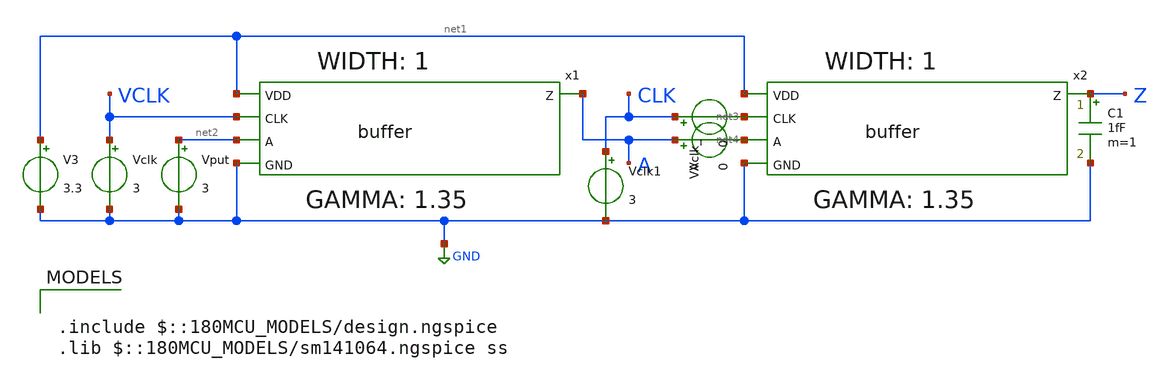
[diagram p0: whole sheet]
** sch_path: xschem/buffer_tb_delay.sch
**.subckt buffer_tb_delay
x2 net1 net3 Z net4 GND buffer
C1 Z GND 1fF m=1
Vput net2 GND 3
Vclk VCLK GND 3
V3 net1 GND 3.3
VA A net4 0
Vclk_ CLK net3 0
Vclk1 CLK GND 3
x1 net1 VCLK A net2 GND buffer
**** begin user architecture code

.include $::180MCU_MODELS/design.ngspice
.lib $::180MCU_MODELS/sm141064.ngspice ss

.control
* [[CITE]] High Performance ASIC Design: Using Synthesizable Domino Logic in an ASIC Flow, by Razak
*+ Hossain.
let vdd = 3.0v $ 3.0v at ss, 3.3v at typical, 3.6v at ff
let vhi = vdd * 0.8
let vlo = vdd * 0.2
let vtrip_fall = vdd * 0.6
let vtrip_rise = vdd * 0.4
let delay = 400ps
let pulse = 1400ps
let clock_pulse = delay + pulse
let temp = -40 $ -40 at ss, 25 at typical, 125 at ff
let tnom = 25

option temp=$&temp tnom=$&tnom

* 3.5.1 Cell delay and output transition time measurement:
* - Initially, all inputs are kept high.
* - The clock is then forced low.
* - After 400ps, all the data inputs are also driven low.
* - The output of a domino only goes low when the clock falls.
*   The fall delay for the cell is measured from the falling edge of the clock input.
* - To measure the rise delay, the related pins rise with the clock.
*   All other data pins remain off.
*   The PUT rises 200ps later.
* - For rise delay measurement from the clock pin, all relative pins rise at the same time as the
*+ clock.
* - The maximum input and clock transition used for characterisation is 150ps.
*   (a 150ps transition from 20% to 80% of Vdd is equivalent to a 250ps 0V to Vdd transition)
* - The maximum cell load used is the maximum capacitance value for the particular drive.
*   The maximum capacitance value is the capacitance load that leads to a 400ps (0 to 100% of Vdd)
*+ falling transition for a domino cell.
* - The delay and transition simulations are done for five different output loads and five different
*+ input transition times.

* 3.5.2 Input pin capacitance measurement
* - The input pin capacitance is measured by taking the integral of the current of the PUT's driving source and dividing it by Vdd.
*   Current is measured only when the signal is rising, and is recorded for each of the 25 delay measurement runs.
*   The average of all these values is then used.

* find maximum capacitance value for the cell
* => binary search on output capacitance such that trans_fall = 400ps
let c_max = 0.2pF
let c_min = 0pF
let c_out = c_min

let target_time = 400ps
let tolerance = 0.1ps
repeat
  set transition_time = 250ps
  let c_test = \{(c_max + c_min) / 2\}
  alter C1 cap = $&c_test
  alter Vclk pulse = [ $&vdd 0.0v 0s $transition_time $transition_time $&clock_pulse 100ns ]
  alter Vclk1 pulse = [ $&vdd 0.0v 0s $transition_time $transition_time $&clock_pulse 100ns ]
  alter Vput pulse = [ $&vdd 0.0v $&delay $transition_time $transition_time $&pulse 100ns ]
  tran 1ps 3ns
  meas tran trans_fall TRIG v(z) VAL=vhi FALL=1 TARG v(z) VAL=vlo FALL=1
  let abs_diff = \{abs(trans_fall - target_time)\}
  if abs_diff < tolerance
    let c_out = c_test
    break
  end
  if trans_fall > target_time
    let c_max = c_test
  else
    let c_min = c_test
  end
  reset
  option temp=$&temp tnom=$&tnom
end

echo -n > out.csv

echo output_cap z \{$&c_out\} >> out.csv

* characterise rise and fall delay and transition times
foreach capacitance_mul 0.2 0.4 0.6 0.8 1.0
  foreach transition_time 50ps 100ps 150ps 200ps 250ps
* input pin characterisation
    let transition_time = $transition_time
    let cap = c_out * $capacitance_mul
    alter C1 cap = $&cap
    alter Vclk pulse = [ $&vdd 0.0v 0s $&transition_time $&transition_time $&clock_pulse 100ns ]
    alter Vclk1 pulse = [ $&vdd 0.0v 0s $&transition_time $&transition_time $&clock_pulse 100ns ]
    alter Vput pulse = [ $&vdd 0.0v $&delay $&transition_time $&transition_time $&pulse 100ns ]
    tran 1ps 3ns

    meas tran delay_rise TRIG v(a) VAL=vtrip_rise RISE=1 TARG v(z) VAL=vtrip_rise RISE=1
    meas tran trans_fall TRIG v(z) VAL=vhi FALL=1 TARG v(z) VAL=vlo FALL=1
    meas tran trans_rise TRIG v(z) VAL=vlo RISE=1 TARG v(z) VAL=vhi RISE=1
    meas tran rise_start WHEN v(a)=vlo RISE=1
    meas tran rise_stop WHEN v(a)=vhi RISE=1
    meas tran charge INTEG i(VA) FROM=rise_start TO=rise_stop

    let transition_time = $transition_time
    let output_cap = c_out * $capacitance_mul
    let input_cap = charge / (vhi - vlo)

    echo delay_rise a z \{$&output_cap\} \{$&transition_time\} \{$&delay_rise\} >> out.csv
    echo trans_fall a z \{$&output_cap\} \{$&transition_time\} \{$&trans_fall\} >> out.csv
    echo trans_rise a z \{$&output_cap\} \{$&transition_time\} \{$&trans_rise\} >> out.csv
    echo input_cap a \{$&output_cap\} \{$&transition_time\} \{$&input_cap\} >> out.csv
    reset
    option temp=$&temp tnom=$&tnom

* clock characterisation
    let transition_time = $transition_time
    let cap = c_out * $capacitance_mul
    alter C1 cap = $&cap
    alter Vclk pulse = [ $&vdd 0.0v 0s $&transition_time $&transition_time $&clock_pulse 100ns ]
    alter Vclk1 pulse = [ $&vdd 0.0v 0s $&transition_time $&transition_time $&clock_pulse 100ns ]
    alter Vput pulse = [ $&vdd 0.0v 0s $&transition_time $&transition_time $&clock_pulse 100ns ]
    tran 1ps 3ns
    meas tran delay_fall TRIG v(clk) VAL=vtrip_fall FALL=1 TARG v(z) VAL=vtrip_fall FALL=1
    meas tran delay_rise TRIG v(clk) VAL=vtrip_rise RISE=1 TARG v(z) VAL=vtrip_rise RISE=1
    meas tran trans_fall TRIG v(z) VAL=vhi FALL=1 TARG v(z) VAL=vlo FALL=1
    meas tran trans_rise TRIG v(z) VAL=vlo RISE=1 TARG v(z) VAL=vhi RISE=1
    meas tran rise_start WHEN v(clk)=vlo RISE=1
    meas tran rise_stop WHEN v(clk)=vhi RISE=1
    meas tran charge INTEG i(VCLK_) FROM=rise_start TO=rise_stop

    let transition_time = $transition_time
    let output_cap = c_out * $capacitance_mul
    let input_cap = charge / (vhi - vlo)
    echo delay_fall clk z \{$&output_cap\} \{$&transition_time\} \{$&delay_fall\} >> out.csv
    echo delay_rise clk z \{$&output_cap\} \{$&transition_time\} \{$&delay_rise\} >> out.csv
    echo trans_fall clk z \{$&output_cap\} \{$&transition_time\} \{$&trans_fall\} >> out.csv
    echo trans_rise clk z \{$&output_cap\} \{$&transition_time\} \{$&trans_rise\} >> out.csv
    echo input_cap clk \{$&output_cap\} \{$&transition_time\} \{$&input_cap\} >> out.csv

    reset
    option temp=$&temp tnom=$&tnom
  end
end

* 3.5.3 Setup measurement of data input rising relative to the clock falling
* - The setup is defined to occur when the output fall delay decreases by 2.5% compared with the fall delays generated by a very large data setup time.
* - The clock initially goes low.
* - Related pins fall soon after.
* - Related pins and clock then rise simultaneously.
* - After a delay, the pin under test rises just before the clock falls.
* - This delay time when the PUT rises is then varied until the output fall delay is 97.5% of the original fall delay.

* characterise setup rise delay
* => binary search on setup such that pulse_width = delay_fall * 0.975
foreach transition_time 83ps 166ps 250ps
  foreach capacitance_mul 0.33 0.66 1.0
    set setup_max = 2000ps
    set setup_min = 260ps
    repeat 14 $ 0.106ps accuracy
      reset
      option temp=$&temp tnom=$&tnom

      let setup = ($setup_max + $setup_min) / 2.0
      let setup_time = 1400ps + (2000ps - setup)
      let transition_time = $transition_time
      let cap = c_out * $capacitance_mul
      alter C1 cap = $&cap
      alter Vclk pulse = [ $&vdd 0.0v 0s 250ps $&transition_time $&clock_pulse 3800ps ]
      alter Vclk1 pulse = [ $&vdd 0.0v 0s 250ps $&transition_time $&clock_pulse 3800ps ]
      alter Vput pulse = [ $&vdd 0.0v 400ps $&transition_time 250ps $&setup_time 100ns ]

      tran 1ps 5ns

      meas tran delay_fall TRIG v(clk) VAL=vtrip_fall FALL=1 TARG v(z) VAL=vtrip_fall FALL=1
      meas tran pulse_width TRIG v(z) VAL=vtrip_rise RISE=1 TARG v(z) VAL=vtrip_fall FALL=2
      meas tran setup_time TRIG v(a) VAL=vtrip_rise RISE=1 TARG v(clk) VAL=vtrip_fall FALL=2

      let pulse_width_target = delay_fall * 0.975
      let abs_diff = \{abs(pulse_width_target - pulse_width)\}
      if abs_diff < tolerance
        break
      end

      if pulse_width > pulse_width_target
        let _setup_max = ($setup_max + $setup_min) / 2.0
        set setup_max = $&_setup_max
      else
        let _setup_min = ($setup_max + $setup_min) / 2.0
        set setup_min = $&_setup_min
      end
    end

    let transition_time = $transition_time
    let output_cap = c_out * $capacitance_mul
    echo setup_rise_vs_clk_fall clk a \{$&output_cap\} \{$&transition_time\} \{$&setup_time\} >> out.csv
  end
end

* 3.5.5 Data pin hold falling measurement
* - The definition of hold time is the time between clock rising (measured at 40% of Vdd) and data input falling (measured at 60% of Vdd) that will cause the evaluation node of the PUT's
*+ cell just to drop below 20 mV.
* - The related pins are chosen to cause the longest delay for PUT.
* - The hold check is done using two extreme clock rise times and two extreme data fall times (four
*+ data points).
* - Output loading is set to the maximum cell loading to ensure worst-case tolerance.

* => binary search on hold time such that min(x2.n0) < 20mV
foreach clock_transition 12ps 250ps
foreach data_transition 12ps 250ps

set hold_max = 4000ps
set hold_min = 0ps
set hold_out = 4000ps

repeat 15 $ 0.122ps accuracy
  reset
  option temp=$&temp tnom=$&tnom

  let hold_time = ($hold_max + $hold_min) / 2.0
  alter C1 cap = $&c_out
  alter Vclk pulse = [ 0.0v $&vdd 1400ps $clock_transition $clock_transition 1000ps 100ns ]
  alter Vclk1 pulse = [ 0.0v $&vdd 2000ps $clock_transition $clock_transition 100ns 100ns ]
  alter Vput pulse = [ $&vdd 0.0v $&hold_time $data_transition $data_transition 100ns 100ns ]

  tran 1ps 5ns

  meas tran hold_time TRIG v(clk) VAL=vtrip_rise RISE=1 TARG v(a) VAL=vtrip_fall FALL=1
  meas tran n0_voltage_max MAX v(x2.n0) from=0ns
  meas tran n0_voltage_min MIN v(x2.n0) from=0ns

  let n0_voltage_target = 20mv

  if n0_voltage_min < n0_voltage_target
    let _hold_max = ($hold_max + $hold_min) / 2.0
    set hold_max = $&_hold_max
    if hold_time < $hold_out
      set hold_out = $&hold_time
    end
  else
    let _hold_min = ($hold_max + $hold_min) / 2.0
    set hold_min = $&_hold_min
  end
end

let clock_transition = $clock_transition
let data_transition = $data_transition
echo hold_fall_vs_clk_rise clk a {$&c_out} {$&clock_transition} {$&data_transition} {$hold_out} >> out.csv

end
end

* 3.5.6 Data pin setup falling [relative to the clock rising] measurement
* - The setup time is defined by measuring the distance between the input and clock pin of the cell
*+ so that they intersect at 20% of Vdd.
* - Two input data pin transition values and two values of clock rise transition times (four points)
*+ are used to build the setup table.

foreach clock_transition 12ps 250ps
  foreach data_transition 12ps 250ps

  set setup_max = 4000ps
  set setup_min = 0ps
  set setup_out = 1000ps

repeat 15 $ 0.122ps accuracy
  reset
  option temp=$&temp tnom=$&tnom

  let setup_time = ($setup_max + $setup_min) / 2.0
  let transition_time = 250ps
  alter C1 cap = $&c_out
  alter Vclk pulse = [ 0.0v $&vdd 1400ps $clock_transition $clock_transition 1000ps 100ns ]
  alter Vclk1 pulse = [ 0.0v $&vdd $&setup_time $clock_transition $clock_transition 100ns 100ns ]
  alter Vput pulse = [ 0.0v $&vdd 1600ps $data_transition $data_transition 100ns 100ns ]

  print setup_time
  tran 1ps 5ns

  let vdd20 = vdd * 0.2

  meas tran vclk20 WHEN v(clk)=$&vdd20 RISE=1
  meas tran va20 WHEN v(a)=$&vdd20 FALL=1
  meas tran setup_time TRIG v(a) VAL=vtrip_fall FALL=1 TARG v(clk) VAL=vtrip_rise RISE=1

  if vclk20 > va20
    let _setup_max = ($setup_max + $setup_min) / 2.0
    set setup_max = $&_setup_max
  else
    let _setup_min = ($setup_max + $setup_min) / 2.0
    set setup_min = $&_setup_min
  end
end

  let clock_transition = $clock_transition
  let data_transition = $data_transition
  echo setup_fall_vs_clk_rise clk a {$&c_out} {$&clock_transition} {$&data_transition} {$&setup_time}
+ >> out.csv
  end
end

* 3.5.7 Minimum clock pulse width for low and high phases
* - For our purposes this check is characterized assuming the maximum clock transitions specified in
*+ the library and the maximum output loading for the cell in question.
* - The minimum pulse width checks are performed by initially setting high the data pins that cause
*+ the longest evaluation delay.
* - The clock is then forced high.
* - The MPWH is measured from when the clock reaches 40% of Vdd, until when the output of the domino
*+ cell reaches 95% of Vdd.
* - MPWL is measured from when the falling clock reaches 60% of Vdd until when the output reaches 5%
*+ of Vdd

reset
option temp=$&temp tnom=$&tnom

let setup_time = ($setup_max + $setup_min) / 2.0
let transition_time = 250ps
alter C1 cap = $&c_out
alter Vclk pulse = [ 0.0v $&vdd 400ps 250ps 250ps 2000ps 100ns ]
alter Vclk1 pulse = [ 0.0v $&vdd 650ps 250ps 250ps 1000ps 100ns ]
alter Vput dc = $&vdd

print setup_time
tran 1ps 5ns

let vdd40 = vdd * 0.40
let vdd60 = vdd * 0.60
let vdd95 = vdd * 0.95
let vdd05 = vdd * 0.05

meas tran mpwh TRIG v(clk) VAL=$&vdd40 RISE=1 TARG v(z) VAL=$&vdd95 RISE=1
meas tran mpwl TRIG v(clk) VAL=$&vdd60 FALL=1 TARG v(z) VAL=$&vdd05 FALL=1

echo min_pulse_width_high clk z {$&mpwh} >> out.csv
echo min_pulse_width_low clk z {$&mpwl} >> out.csv

* 3.5.10 Precharge sizing check
* - The precharge sizing check involves making sure that the internal node of the domino cells
*+ reaches at least 90% of Vdd at maximum frequency

foreach clock_transition 12ps 250ps

  reset
  option temp=$&temp tnom=$&tnom

  alter C1 cap = $&c_out
  alter Vclk dc = 0.0v
  alter Vclk1 pulse = [ $&vdd 0.0v 200ps $clock_transition $clock_transition 400ps 100ns ]
  alter Vput dc = 0.0v

  tran 1ps 1ns

  meas tran max_voltage MAX v(x2.n0) from=0ps

  let vdd90 = vdd * 0.9
  let clock_transition = $clock_transition
  let precharge_check = (max_voltage gt vdd90) ? 1 : 0
  echo precharge_check {$&clock_transition} {$&precharge_check} >> out.csv

end

rusage

exit

.endc

**** end user architecture code
**.ends

* expanding   symbol:  buffer.sym # of pins=5
** sym_path: xschem/buffer.sym
** sch_path: xschem/buffer.sch
.subckt buffer VDD CLK Z A GND
*.ipin A
*.ipin CLK
*.ipin VDD
*.ipin GND
*.opin Z
XM1 N0 A net1 GND nfet_03v3 L=0.28u W=0.60u nf=1 ad='int((nf+1)/2) * W/nf * 0.18u' as='int((nf+2)/2) * W/nf * 0.18u'
+ pd='2*int((nf+1)/2) * (W/nf + 0.18u)' ps='2*int((nf+2)/2) * (W/nf + 0.18u)' nrd='0.18u / W' nrs='0.18u / W'
+ sa=0 sb=0 sd=0 m=1
XM2 net1 CLK GND GND nfet_03v3 L=0.28u W=0.60u nf=1 ad='int((nf+1)/2) * W/nf * 0.18u' as='int((nf+2)/2) * W/nf * 0.18u'
+ pd='2*int((nf+1)/2) * (W/nf + 0.18u)' ps='2*int((nf+2)/2) * (W/nf + 0.18u)' nrd='0.18u / W' nrs='0.18u / W'
+ sa=0 sb=0 sd=0 m=1
XM3 N0 CLK VDD VDD pfet_03v3 L=0.28u W=0.30u nf=1 ad='int((nf+1)/2) * W/nf * 0.18u' as='int((nf+2)/2) * W/nf * 0.18u'
+ pd='2*int((nf+1)/2) * (W/nf + 0.18u)' ps='2*int((nf+2)/2) * (W/nf + 0.18u)' nrd='0.18u / W' nrs='0.18u / W'
+ sa=0 sb=0 sd=0 m=1
XM4 Z N0 VDD VDD pfet_03v3 L=0.28u W=0.41u nf=1 ad='int((nf+1)/2) * W/nf * 0.18u' as='int((nf+2)/2) * W/nf * 0.18u'
+ pd='2*int((nf+1)/2) * (W/nf + 0.18u)' ps='2*int((nf+2)/2) * (W/nf + 0.18u)' nrd='0.18u / W' nrs='0.18u / W'
+ sa=0 sb=0 sd=0 m=1
XM5 Z N0 GND GND nfet_03v3 L=0.28u W=0.30u nf=1 ad='int((nf+1)/2) * W/nf * 0.18u' as='int((nf+2)/2) * W/nf * 0.18u'
+ pd='2*int((nf+1)/2) * (W/nf + 0.18u)' ps='2*int((nf+2)/2) * (W/nf + 0.18u)' nrd='0.18u / W' nrs='0.18u / W'
+ sa=0 sb=0 sd=0 m=1
XM6 N0 Z VDD VDD pfet_03v3 L=0.28u W=0.30u nf=1 ad='int((nf+1)/2) * W/nf * 0.18u' as='int((nf+2)/2) * W/nf * 0.18u'
+ pd='2*int((nf+1)/2) * (W/nf + 0.18u)' ps='2*int((nf+2)/2) * (W/nf + 0.18u)' nrd='0.18u / W' nrs='0.18u / W'
+ sa=0 sb=0 sd=0 m=1
.ends

.GLOBAL GND
.end
